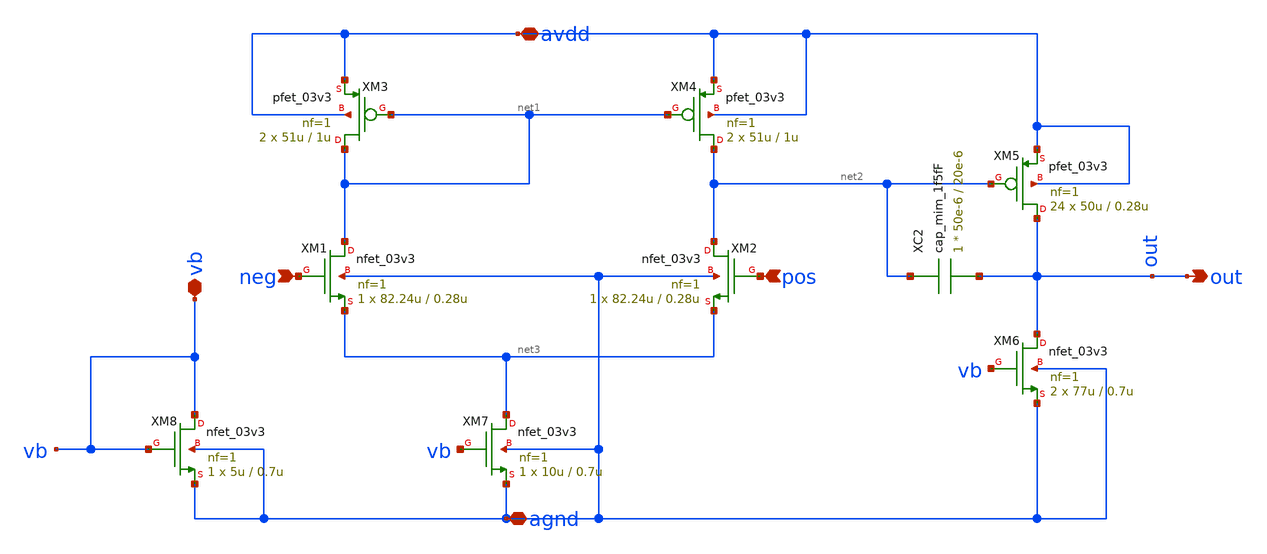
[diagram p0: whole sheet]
** sch_path: LDO/xschem/ota-ldo/ota-ldo.sch
**.subckt ota-ldo vb avdd agnd neg pos out
*.iopin vb
*.iopin avdd
*.iopin agnd
*.ipin neg
*.ipin pos
*.opin out
XC2 net2 out cap_mim_1f5fF c_width=50e-6 c_length=20e-6 m=1
XM1 net1 neg net3 agnd nfet_03v3 L=0.28u W=82.24u nf=1 ad='int((nf+1)/2) * W/nf * 0.18u' as='int((nf+2)/2) * W/nf * 0.18u'
+ pd='2*int((nf+1)/2) * (W/nf + 0.18u)' ps='2*int((nf+2)/2) * (W/nf + 0.18u)' nrd='0.18u / W' nrs='0.18u / W'
+ sa=0 sb=0 sd=0 m=1
XM3 net1 net1 avdd avdd pfet_03v3 L=1u W=51u nf=1 ad='int((nf+1)/2) * W/nf * 0.18u' as='int((nf+2)/2) * W/nf * 0.18u'
+ pd='2*int((nf+1)/2) * (W/nf + 0.18u)' ps='2*int((nf+2)/2) * (W/nf + 0.18u)' nrd='0.18u / W' nrs='0.18u / W'
+ sa=0 sb=0 sd=0 m=2
XM2 net2 pos net3 agnd nfet_03v3 L=0.28u W=82.24u nf=1 ad='int((nf+1)/2) * W/nf * 0.18u' as='int((nf+2)/2) * W/nf * 0.18u'
+ pd='2*int((nf+1)/2) * (W/nf + 0.18u)' ps='2*int((nf+2)/2) * (W/nf + 0.18u)' nrd='0.18u / W' nrs='0.18u / W'
+ sa=0 sb=0 sd=0 m=1
XM4 net2 net1 avdd avdd pfet_03v3 L=1u W=51u nf=1 ad='int((nf+1)/2) * W/nf * 0.18u' as='int((nf+2)/2) * W/nf * 0.18u'
+ pd='2*int((nf+1)/2) * (W/nf + 0.18u)' ps='2*int((nf+2)/2) * (W/nf + 0.18u)' nrd='0.18u / W' nrs='0.18u / W'
+ sa=0 sb=0 sd=0 m=2
XM7 net3 vb agnd agnd nfet_03v3 L=0.7u W=10u nf=1 ad='int((nf+1)/2) * W/nf * 0.18u' as='int((nf+2)/2) * W/nf * 0.18u'
+ pd='2*int((nf+1)/2) * (W/nf + 0.18u)' ps='2*int((nf+2)/2) * (W/nf + 0.18u)' nrd='0.18u / W' nrs='0.18u / W'
+ sa=0 sb=0 sd=0 m=1
XM8 vb vb agnd agnd nfet_03v3 L=0.7u W=5u nf=1 ad='int((nf+1)/2) * W/nf * 0.18u' as='int((nf+2)/2) * W/nf * 0.18u'
+ pd='2*int((nf+1)/2) * (W/nf + 0.18u)' ps='2*int((nf+2)/2) * (W/nf + 0.18u)' nrd='0.18u / W' nrs='0.18u / W'
+ sa=0 sb=0 sd=0 m=1
XM5 out net2 avdd avdd pfet_03v3 L=0.28u W=50u nf=1 ad='int((nf+1)/2) * W/nf * 0.18u' as='int((nf+2)/2) * W/nf * 0.18u'
+ pd='2*int((nf+1)/2) * (W/nf + 0.18u)' ps='2*int((nf+2)/2) * (W/nf + 0.18u)' nrd='0.18u / W' nrs='0.18u / W'
+ sa=0 sb=0 sd=0 m=24
XM6 out vb agnd agnd nfet_03v3 L=0.7u W=77u nf=1 ad='int((nf+1)/2) * W/nf * 0.18u' as='int((nf+2)/2) * W/nf * 0.18u'
+ pd='2*int((nf+1)/2) * (W/nf + 0.18u)' ps='2*int((nf+2)/2) * (W/nf + 0.18u)' nrd='0.18u / W' nrs='0.18u / W'
+ sa=0 sb=0 sd=0 m=2
**.ends
.end
